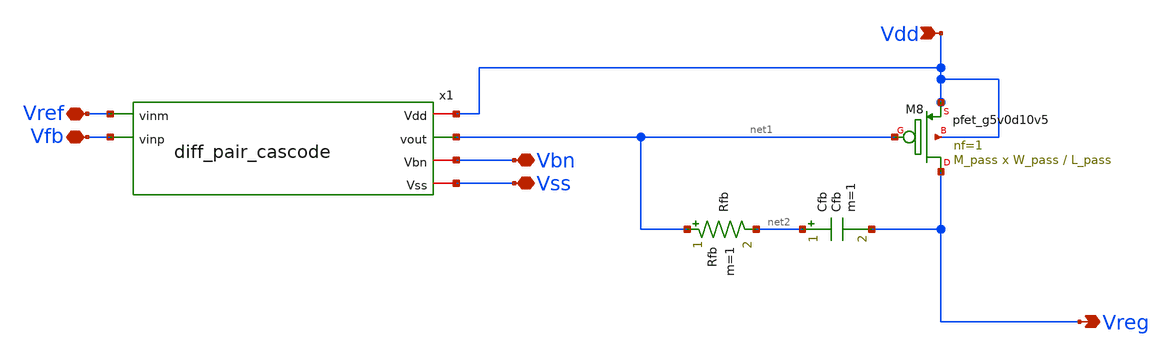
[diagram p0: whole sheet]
** sch_path: xschem/ldo_cascode.sch
**.subckt ldo_cascode Vbn Vss Vreg Vref Vdd Vfb
*.iopin Vbn
*.iopin Vss
*.opin Vreg
*.iopin Vref
*.ipin Vdd
*.iopin Vfb
XM8 Vreg net1 Vdd Vdd sky130_fd_pr__pfet_g5v0d10v5 L=L_pass W=W_pass nf=1 ad='int((nf+1)/2) * W/nf * 0.29'
+ as='int((nf+2)/2) * W/nf * 0.29' pd='2*int((nf+1)/2) * (W/nf + 0.29)' ps='2*int((nf+2)/2) * (W/nf + 0.29)'
+ nrd='0.29 / W' nrs='0.29 / W' sa=0 sb=0 sd=0 mult=M_pass m=M_pass
Rfb net1 net2 Rfb m=1
Cfb net2 Vreg Cfb m=1
x1 Vdd net1 Vref Vfb Vbn Vss diff_pair_cascode
**.ends

* expanding   symbol:  diff_pair_cascode.sym # of pins=6
** sym_path: xschem/diff_pair_cascode.sym
** sch_path: xschem/diff_pair_cascode.sch
.subckt diff_pair_cascode Vdd vout vinm vinp Vbn Vss
*.ipin vinm
*.ipin vinp
*.iopin Vbn
*.opin vout
*.iopin Vss
*.iopin Vdd
XM1 net1 vinp net4 Vss sky130_fd_pr__nfet_g5v0d10v5 L=L_M1 W=W_M1 nf=1 ad='int((nf+1)/2) * W/nf * 0.29'
+ as='int((nf+2)/2) * W/nf * 0.29' pd='2*int((nf+1)/2) * (W/nf + 0.29)' ps='2*int((nf+2)/2) * (W/nf + 0.29)'
+ nrd='0.29 / W' nrs='0.29 / W' sa=0 sb=0 sd=0 mult=1 m=1
XM2 vout vinm net4 Vss sky130_fd_pr__nfet_g5v0d10v5 L=L_M2 W=W_M2 nf=1 ad='int((nf+1)/2) * W/nf * 0.29'
+ as='int((nf+2)/2) * W/nf * 0.29' pd='2*int((nf+1)/2) * (W/nf + 0.29)' ps='2*int((nf+2)/2) * (W/nf + 0.29)'
+ nrd='0.29 / W' nrs='0.29 / W' sa=0 sb=0 sd=0 mult=1 m=1
XM3 vout net1 net3 Vdd sky130_fd_pr__pfet_g5v0d10v5 L=L_M3 W=W_M3 nf=1 ad='int((nf+1)/2) * W/nf * 0.29'
+ as='int((nf+2)/2) * W/nf * 0.29' pd='2*int((nf+1)/2) * (W/nf + 0.29)' ps='2*int((nf+2)/2) * (W/nf + 0.29)'
+ nrd='0.29 / W' nrs='0.29 / W' sa=0 sb=0 sd=0 mult=1 m=1
XM4 net1 net1 net2 Vdd sky130_fd_pr__pfet_g5v0d10v5 L=L_M4 W=W_M4 nf=1 ad='int((nf+1)/2) * W/nf * 0.29'
+ as='int((nf+2)/2) * W/nf * 0.29' pd='2*int((nf+1)/2) * (W/nf + 0.29)' ps='2*int((nf+2)/2) * (W/nf + 0.29)'
+ nrd='0.29 / W' nrs='0.29 / W' sa=0 sb=0 sd=0 mult=1 m=1
XM7 net4 Vbn Vss Vss sky130_fd_pr__nfet_g5v0d10v5 L=L_M7 W=W_M7 nf=1 ad='int((nf+1)/2) * W/nf * 0.29'
+ as='int((nf+2)/2) * W/nf * 0.29' pd='2*int((nf+1)/2) * (W/nf + 0.29)' ps='2*int((nf+2)/2) * (W/nf + 0.29)'
+ nrd='0.29 / W' nrs='0.29 / W' sa=0 sb=0 sd=0 mult=1 m=1
XM5 net3 net2 Vdd Vdd sky130_fd_pr__pfet_g5v0d10v5 L=L_M5 W=W_M5 nf=1 ad='int((nf+1)/2) * W/nf * 0.29'
+ as='int((nf+2)/2) * W/nf * 0.29' pd='2*int((nf+1)/2) * (W/nf + 0.29)' ps='2*int((nf+2)/2) * (W/nf + 0.29)'
+ nrd='0.29 / W' nrs='0.29 / W' sa=0 sb=0 sd=0 mult=1 m=1
XM6 net2 net2 Vdd Vdd sky130_fd_pr__pfet_g5v0d10v5 L=L_M6 W=W_M6 nf=1 ad='int((nf+1)/2) * W/nf * 0.29'
+ as='int((nf+2)/2) * W/nf * 0.29' pd='2*int((nf+1)/2) * (W/nf + 0.29)' ps='2*int((nf+2)/2) * (W/nf + 0.29)'
+ nrd='0.29 / W' nrs='0.29 / W' sa=0 sb=0 sd=0 mult=1 m=1
.ends

.end
